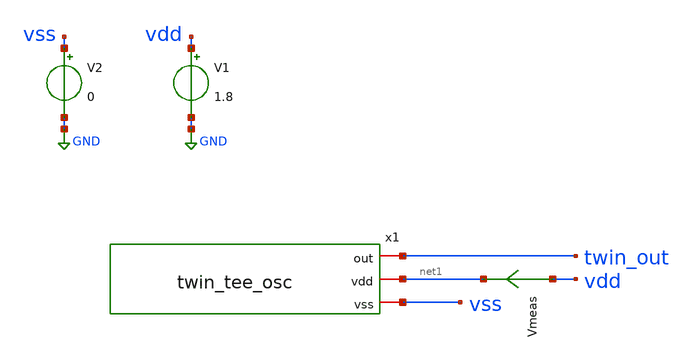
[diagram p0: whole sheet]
** sch_path: xschem/tb_twin_tee_osc.sch
**.subckt tb_twin_tee_osc
V1 vdd GND 1.8
V2 vss GND 0
x1 twin_out net1 vss twin_tee_osc
Vmeas vdd net1 0
**** begin user architecture code

** opencircuitdesign pdks install
.lib $::SKYWATER_MODELS/sky130.lib.spice tt_mm
*.include $::SKYWATER_STDCELLS/sky130_fd_sc_hd.spice





*.option  METHOD = GEAR
*.param mc_mm_switch=0
*.ic v(twin_out)=0.8
.control
repeat 5

  tran 500p 2u uic
  write tb_twin_tee_osc.raw
  set appendwrite
  reset

end
.endc


**** end user architecture code
**.ends

* expanding   symbol:  twin_tee_osc.sym # of pins=3
** sym_path: xschem/twin_tee_osc.sym
** sch_path: xschem/twin_tee_osc.sch
.subckt twin_tee_osc out vdd vss
*.iopin vdd
*.iopin vss
*.iopin out
x1 vdd net2 net1 out vss p3_opamp
x2 vdd vss out net2 twin_tee
XR2 out net1 vss sky130_fd_pr__res_high_po_0p35 L=500 mult=1 m=1
XR4 vss net1 vss sky130_fd_pr__res_high_po_0p35 L=10 mult=1 m=1
XR1 net1 vdd vss sky130_fd_pr__res_high_po_0p35 L=10 mult=1 m=1
.ends


* expanding   symbol:  p3_opamp.sym # of pins=5
** sym_path: p3_opamp.sym
** sch_path: p3_opamp.sch
.subckt p3_opamp VDD MINUS PLUS VOUT VSS
*.iopin VDD
*.iopin VSS
*.iopin PLUS
*.iopin MINUS
*.iopin VOUT
XM3 VX VBIAS VSS VSS sky130_fd_pr__nfet_01v8 L=2 W=4 nf=4 ad='int((nf+1)/2) * W/nf * 0.29' as='int((nf+2)/2) * W/nf * 0.29'
+ pd='2*int((nf+1)/2) * (W/nf + 0.29)' ps='2*int((nf+2)/2) * (W/nf + 0.29)' nrd='0.29 / W' nrs='0.29 / W'
+ sa=0 sb=0 sd=0 mult=1 m=1
XM6 VBIAS VBIAS VSS VSS sky130_fd_pr__nfet_01v8 L=2 W=4 nf=4 ad='int((nf+1)/2) * W/nf * 0.29' as='int((nf+2)/2) * W/nf * 0.29'
+ pd='2*int((nf+1)/2) * (W/nf + 0.29)' ps='2*int((nf+2)/2) * (W/nf + 0.29)' nrd='0.29 / W' nrs='0.29 / W'
+ sa=0 sb=0 sd=0 mult=1 m=1
XM7 VOUT VBIAS VSS VSS sky130_fd_pr__nfet_01v8 L=2 W=7 nf=7 ad='int((nf+1)/2) * W/nf * 0.29' as='int((nf+2)/2) * W/nf * 0.29'
+ pd='2*int((nf+1)/2) * (W/nf + 0.29)' ps='2*int((nf+2)/2) * (W/nf + 0.29)' nrd='0.29 / W' nrs='0.29 / W'
+ sa=0 sb=0 sd=0 mult=1 m=1
XR1 VBIAS VDD VSS sky130_fd_pr__res_xhigh_po_0p35 L=2.9 mult=1 m=1
XM2 V2 MINUS VX VSS sky130_fd_pr__nfet_01v8_lvt L=0.5 W=2.5 nf=1 ad='int((nf+1)/2) * W/nf * 0.29' as='int((nf+2)/2) * W/nf * 0.29'
+ pd='2*int((nf+1)/2) * (W/nf + 0.29)' ps='2*int((nf+2)/2) * (W/nf + 0.29)' nrd='0.29 / W' nrs='0.29 / W'
+ sa=0 sb=0 sd=0 mult=1 m=1
XM1 V1 PLUS VX VSS sky130_fd_pr__nfet_01v8_lvt L=0.5 W=2.5 nf=1 ad='int((nf+1)/2) * W/nf * 0.29' as='int((nf+2)/2) * W/nf * 0.29'
+ pd='2*int((nf+1)/2) * (W/nf + 0.29)' ps='2*int((nf+2)/2) * (W/nf + 0.29)' nrd='0.29 / W' nrs='0.29 / W'
+ sa=0 sb=0 sd=0 mult=1 m=1
XM4 V2 V2 VDD VDD sky130_fd_pr__pfet_01v8_lvt L=2 W=6 nf=6 ad='int((nf+1)/2) * W/nf * 0.29' as='int((nf+2)/2) * W/nf * 0.29'
+ pd='2*int((nf+1)/2) * (W/nf + 0.29)' ps='2*int((nf+2)/2) * (W/nf + 0.29)' nrd='0.29 / W' nrs='0.29 / W'
+ sa=0 sb=0 sd=0 mult=1 m=1
XM5 V1 V2 VDD VDD sky130_fd_pr__pfet_01v8_lvt L=2 W=6 nf=6 ad='int((nf+1)/2) * W/nf * 0.29' as='int((nf+2)/2) * W/nf * 0.29'
+ pd='2*int((nf+1)/2) * (W/nf + 0.29)' ps='2*int((nf+2)/2) * (W/nf + 0.29)' nrd='0.29 / W' nrs='0.29 / W'
+ sa=0 sb=0 sd=0 mult=1 m=1
XM8 VOUT V1 VDD VDD sky130_fd_pr__pfet_01v8_lvt L=0.5 W=20 nf=20 ad='int((nf+1)/2) * W/nf * 0.29' as='int((nf+2)/2) * W/nf * 0.29'
+ pd='2*int((nf+1)/2) * (W/nf + 0.29)' ps='2*int((nf+2)/2) * (W/nf + 0.29)' nrd='0.29 / W' nrs='0.29 / W'
+ sa=0 sb=0 sd=0 mult=1 m=1
.ends


* expanding   symbol:  twin_tee.sym # of pins=4
** sym_path: xschem/twin_tee.sym
** sch_path: xschem/twin_tee.sch
.subckt twin_tee vdd vss out in
*.iopin vdd
*.iopin vss
*.iopin in
*.iopin out
XR4 c1_c2 out vss sky130_fd_pr__res_high_po_0p35 L=40 mult=1 m=1
XC1 c1_c2 vss sky130_fd_pr__cap_mim_m3_1 W=15 L=15 MF=1 m=1
XC2 c1_c2 vss sky130_fd_pr__cap_mim_m3_1 W=15 L=15 MF=1 m=1
XR5 in c1_c2 vss sky130_fd_pr__res_high_po_0p35 L=40 mult=1 m=1
XC3 c3_c4 in sky130_fd_pr__cap_mim_m3_1 W=15 L=15 MF=1 m=1
XC4 out c3_c4 sky130_fd_pr__cap_mim_m3_1 W=15 L=15 MF=1 m=1
XR6 c3_c4 vss vss sky130_fd_pr__res_high_po_0p35 L=20 mult=1 m=1
.ends

.GLOBAL GND
.end
